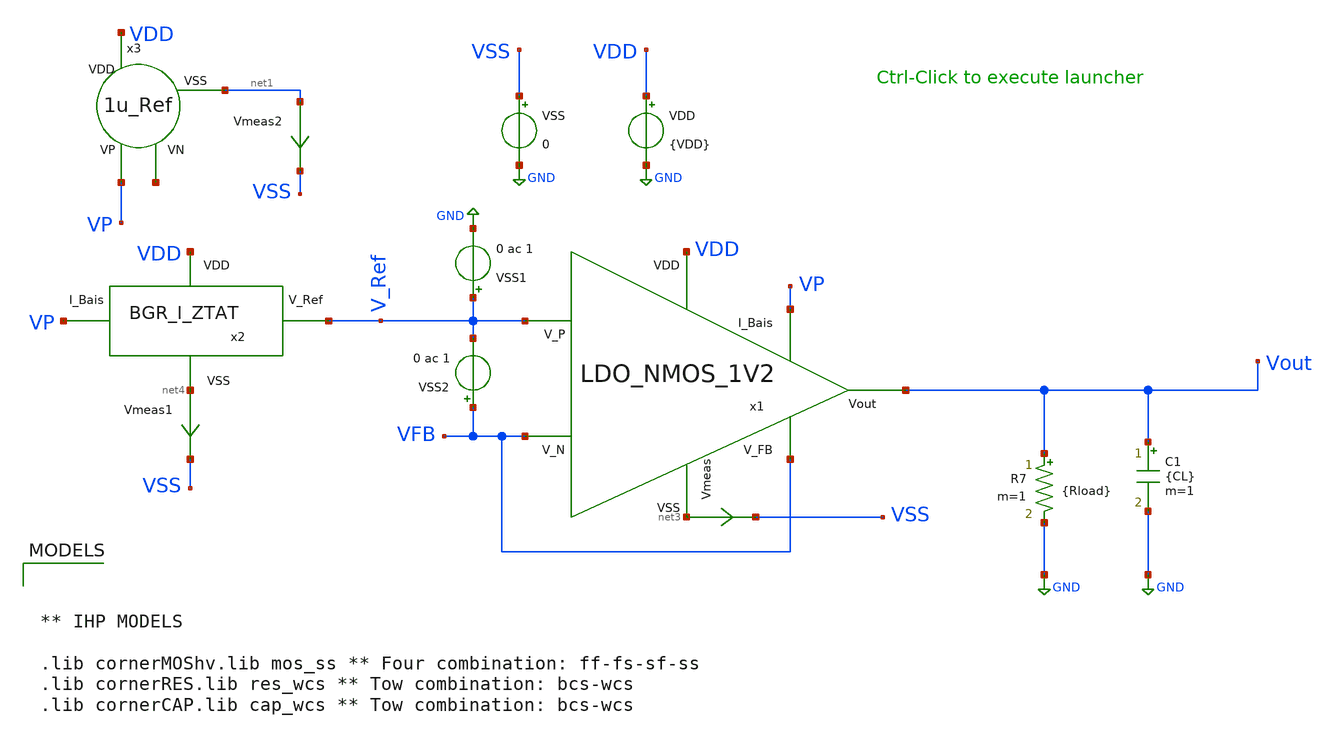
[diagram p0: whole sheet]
** sch_path: dependencies/PMU/PMU-main/testbenches/corners/xschem/PMU_AC_Stability_TB_Corners.sch
**.subckt PMU_AC_Stability_TB_Corners
VDD VDD GND {VDD}
Vmeas2 net1 VSS 0
.save i(vmeas2)
VSS VSS GND 0
C1 Vout GND {CL} m=1
R7 Vout GND {Rload} m=1
x3 VDD VP net2 net1 1u_Ref
x1 VDD VP V_Ref VFB Vout VFB net3 LDO_NMOS_1V2
Vmeas net3 VSS 0
.save i(vmeas)
Vmeas1 net4 VSS 0
.save i(vmeas1)
x2 VDD net4 V_Ref VP BGR_I_ZTAT
VSS1 V_Ref GND 0 ac 1
VSS2 VFB V_Ref 0 ac 1
**** begin user architecture code


.save all
.options rshunt = 1e12
.options gmin=1e-12
.options reltol=0.01 abstol=1p
.param temp = 0
.param VDD = 2.2
.param CL=100p
.param Rload=2.4k

.option filetype=ascii
.control
set appendwrite
  let run_n = 0
  let run_t = 0
  let run_v = 0
  let run_c = 0
  let run_r = 0

  let TM = 0
  let VL = 2.2
  let CLL = 50p
  let RL = 2.4k
let mc_runs = 16
let run = 0
set curplot=new
set scratch=$curplot
setplot $scratch

let BW=unitvec(mc_runs)
let Gain=unitvec(mc_runs)
let Phase=unitvec(mc_runs)

let PS=unitvec(mc_runs)
let Tem=unitvec(mc_runs)
let Capa=unitvec(mc_runs)
let Res=unitvec(mc_runs)
dowhile run < mc_runs
reset
	dowhile run_r < 2
	alterparam RLoad={$&RL}
	reset
	dowhile run_c < 2
	alterparam CL={$&CLL}
	reset
	dowhile run_v < 2
	alterparam VDD={$&VL}
	reset
	dowhile run_t < 2
	alterparam temp={$&TM}
	reset


		ac dec 100 1 1g
		let G_P = db(Vout)
		let PH_P = 180*cph(Vout)/Pi
		meas ac UBW when G_P = 0
		meas ac PM FIND PH_P at=UBW
		meas ac G FIND G_P at=1

		set run=$&run
		set dt=$curplot
		setplot $scratch

		let BW[$run]={$dt}.UBW
		let Gain[$run]={$dt}.G
		let Phase[$run]={$dt}.PM
		let PS[$run]={$dt}.VL
		let Tem[$run]={$dt}.TM
		let Capa[$run]={$dt}.CLL
		let Res[$run]={$dt}.RL
		setplot $dt
		let run = run + 1

	let run_t = run_t + 1
	let TM = 85
	end
	let TM = 0
	let run_t = 0

	let run_v = run_v + 1
	let VL = 3.3
	end
	let run_v = 0
	let VL = 2.2

	let run_c = run_c + 1
	let CLL = 150p
	end
	let run_c = 0
	let CLL = 50p

	let run_r = run_r + 1
	let RL = 240k
	end
	let run_r = 0
	let  RL = 2.4k
end

wrdata PMU_AC_Stability_TB_Corners.csv {$scratch}.BW {$scratch}.Gain {$scratch}.Phase {$scratch}.PS {$scratch}.Tem
+ {$scratch}.Capa {$scratch}.Res
write PMU_AC_Stability_TB_Corners.raw
echo
print {$scratch}.BW {$scratch}.Gain {$scratch}.Phase {$scratch}.PS {$scratch}.Tem {$scratch}.Capa {$scratch}.Res
unset appendwrite
.endc





** IHP MODELS

.lib cornerMOShv.lib mos_ss ** Four combination: ff-fs-sf-ss
.lib cornerRES.lib res_wcs ** Tow combination: bcs-wcs
.lib cornerCAP.lib cap_wcs ** Tow combination: bcs-wcs


**** end user architecture code
**.ends

* expanding   symbol:  1u_Ref.sym # of pins=4
** sym_path: dependencies/PMU/PMU-main/schematic/xschem/1u_Ref.sym
** sch_path: dependencies/PMU/PMU-main/schematic/xschem/1u_Ref.sch
.subckt 1u_Ref VDD VP VN VSS
*.iopin VDD
*.iopin VSS
*.iopin VP
*.iopin VN
XM1 VP VP VDD VDD sg13_hv_pmos w=10u l=2u ng=1 m=1 mm_ok=1
XM2 VN VP VDD VDD sg13_hv_pmos w=10u l=2u ng=1 m=1 mm_ok=1
XM6 net1 net1 VDD VDD sg13_hv_pmos w=0.3u l=10u ng=1 m=1 mm_ok=1
XM7 V1 VN net4 net4 sg13_hv_nmos w=1u l=6u ng=1 m=1 mm_ok=1
XM5 net3 V1 VN VSS sg13_hv_nmos w=1u l=10u ng=1 m=1 mm_ok=1
Vmeas2 net2 VSS 0
.save i(vmeas2)
XM4 VN VR net2 net2 sg13_hv_nmos w=10u l=1u ng=1 m=1 mm_ok=1
XM3 net5 VN VR VSS sg13_hv_nmos w=10u l=1u ng=1 m=4 mm_ok=1
Vmeas1 VP net5 0
.save i(vmeas1)
Vmeas3 VP net3 0
.save i(vmeas3)
Vmeas4 net4 VSS 0
.save i(vmeas4)
XM8 V1 V1 net1 VDD sg13_hv_pmos w=0.3u l=10u ng=1 m=1 mm_ok=1
XR1 VR VSS sub! rhigh w=0.5e-6 l=185e-6 m=1 b=0 mm_ok=1
.ends


* expanding   symbol:  LDO_NMOS_1V2.sym # of pins=7
** sym_path: dependencies/PMU/PMU-main/schematic/xschem/LDO_NMOS_1V2.sym
** sch_path: dependencies/PMU/PMU-main/schematic/xschem/LDO_NMOS_1V2.sch
.subckt LDO_NMOS_1V2 VDD I_Bais V_P V_N Vout V_FB VSS
*.iopin Vout
*.iopin VDD
*.iopin I_Bais
*.iopin V_P
*.iopin V_N
*.iopin V_FB
*.iopin VSS
Vmeas net6 VSS 0
.save i(vmeas)
XM6 VDD VG2 Vout GND sg13_hv_nmos w=10u l=0.45u ng=10 m=50 mm_ok=1
XR3 Vout V_FB sub! rhigh w=0.5e-6 l=18e-6 m=2 b=0 mm_ok=1
Vmeas1 net5 VSS 0
.save i(vmeas1)
XR2 V_FB net3 sub! rhigh w=0.5e-6 l=18e-6 m=2 b=0 mm_ok=1
XR4 net3 net2 sub! rhigh w=0.5e-6 l=18e-6 m=2 b=0 mm_ok=1
XR5 net2 net5 sub! rhigh w=0.5e-6 l=18e-6 m=2 b=0 mm_ok=1
x1 VDD I_Bais V_N V_P net1 VG2 net6 OpAmp_2etags
XC3 net4 net1 cap_cmim w=33.24e-6 l=50.0e-6 m=3 mm_ok=1
XC4 VG2 net5 cap_cmim w=33.24e-6 l=50e-6 m=2 mm_ok=1
XR1 VG2 net4 sub! rhigh w=0.5e-6 l=15e-6 m=1 b=0 mm_ok=1
.ends


* expanding   symbol:  /foss/designs/bgr/BGR_I_ZTAT.sym # of pins=4
** sym_path: dependencies/PMU/PMU-main/schematic/xschem/BGR_I_ZTAT.sym
** sch_path: dependencies/PMU/PMU-main/schematic/xschem/BGR_I_ZTAT.sch
.subckt BGR_I_ZTAT VDD VSS V_Ref I_Bais
*.iopin VDD
*.iopin I_Bais
*.iopin V_Ref
*.iopin VSS
XM7 net2 V_out VDD VDD sg13_hv_pmos w=1u l=3u ng=1 m=1 mm_ok=1
XM8 net3 V_out VDD VDD sg13_hv_pmos w=1u l=3u ng=1 m=1 mm_ok=1
XC1 VDD V_out cap_cmim w=13.265e-6 l=50e-6 m=1 mm_ok=1
Vmeas1 net3 Vp 0
.save i(vmeas1)
Vmeas22 Vn net1 0
.save i(vmeas22)
x2 VDD I_Bais Vp Vn V_out net5 Stage1
XM2 Vp1 Vp1 VSS VSS sg13_hv_nmos w=7.5u l=4u ng=1 m=2 mm_ok=1
XM3 net1 net1 VSS VSS sg13_hv_nmos w=7.5u l=4u ng=1 m=1 mm_ok=1
Vmeas2 net2 Vn 0
.save i(vmeas2)
Vmeas5 net4 Vp1 0
.save i(vmeas5)
Vmeas6 net5 VSS 0
.save i(vmeas6)
XM1 V_Ref V_out VDD VDD sg13_hv_pmos w=1u l=3u ng=1 m=1 mm_ok=1
Vmeas3 V_Ref net11 0
.save i(vmeas3)
XM4 net11 net11 VSS VSS sg13_hv_nmos w=2u l=2.75u ng=1 m=1 mm_ok=1
XM6 net8 Vn VSS GND sg13_hv_nmos w=4u l=2u ng=1 m=1 mm_ok=1
XM5 net6 net6 VDD VDD sg13_hv_pmos w=4u l=1u ng=1 m=1 mm_ok=1
XM9 net7 net6 VDD VDD sg13_hv_pmos w=4u l=1u ng=1 m=1 mm_ok=1
Vmeas4 net7 net8 0
.save i(vmeas4)
XC3 net9 VSS cap_cmim w=5e-6 l=5e-6 m=1 mm_ok=1
XM10 VSS VDD net6 VDD sg13_hv_pmos w=4u l=1u ng=1 m=1 mm_ok=1
XMSU V_out net8 net10 net10 sg13_hv_nmos w=4u l=2u ng=1 m=1 mm_ok=1
Vmeas8 net6 net9 0
.save i(vmeas8)
Vmeas9 net10 VSS 0
.save i(vmeas9)
XR4 Vp VSS sub! rhigh w=0.5e-6 l=80e-6 m=1 b=0 mm_ok=1
XR5 Vp net4 sub! rhigh w=0.5e-6 l=210e-6 m=1 b=0 mm_ok=1
.ends


* expanding   symbol:  OpAmp_2etags.sym # of pins=7
** sym_path: dependencies/PMU/PMU-main/schematic/xschem/OpAmp_2etags.sym
** sch_path: dependencies/PMU/PMU-main/schematic/xschem/OpAmp_2etags.sch
.subckt OpAmp_2etags VDD I_Bais VP VN VG VOUT VSS
*.iopin VDD
*.iopin I_Bais
*.iopin VP
*.iopin VN
*.iopin VG
*.iopin VOUT
*.iopin VSS
XM3 VX2 VX2 VSS VSS sg13_hv_nmos w=10u l=2u ng=1 m=2 mm_ok=1
XM1 VX2 VP net1 VDD sg13_hv_pmos w=5u l=2u ng=1 m=2 mm_ok=1
XM2 VG VN net1 VDD sg13_hv_pmos w=5u l=2u ng=1 m=2 mm_ok=1
XM4 VG VX2 VSS VSS sg13_hv_nmos w=10u l=2u ng=1 m=2 mm_ok=1
XM5 net1 I_Bais VDD VDD sg13_hv_pmos w=10u l=2u ng=1 m=4 mm_ok=1
XM7 VOUT I_Bais VDD VDD sg13_hv_pmos w=10u l=2u ng=1 m=8 mm_ok=1
XM6 VOUT VG VSS VSS sg13_hv_nmos w=10u l=2u ng=1 m=8 mm_ok=1
.ends


* expanding   symbol:  Stage1.sym # of pins=6
** sym_path: dependencies/PMU/PMU-main/schematic/xschem/Stage1.sym
** sch_path: dependencies/PMU/PMU-main/schematic/xschem/Stage1.sch
.subckt Stage1 VDD VB Vin1 Vin2 Vout1 VSS
*.iopin VDD
*.ipin VB
*.ipin Vin1
*.ipin Vin2
*.iopin VSS
*.opin Vout1
XM1 net1 Vin1 VX VDD sg13_hv_pmos w=10u l=5u ng=2 m=2 mm_ok=1
XM2 net1 net1 VSS VSS sg13_hv_nmos w=1u l=10u ng=2 m=2 mm_ok=1
XM3 Vout1 net1 VSS VSS sg13_hv_nmos w=1u l=10u ng=2 m=2 mm_ok=1
XM4 Vout1 Vin2 VX VDD sg13_hv_pmos w=10u l=5u ng=2 m=2 mm_ok=1
XM5 VX VB VDD VDD sg13_hv_pmos w=10u l=2u ng=1 m=5 mm_ok=1
.ends

.GLOBAL GND
.end
